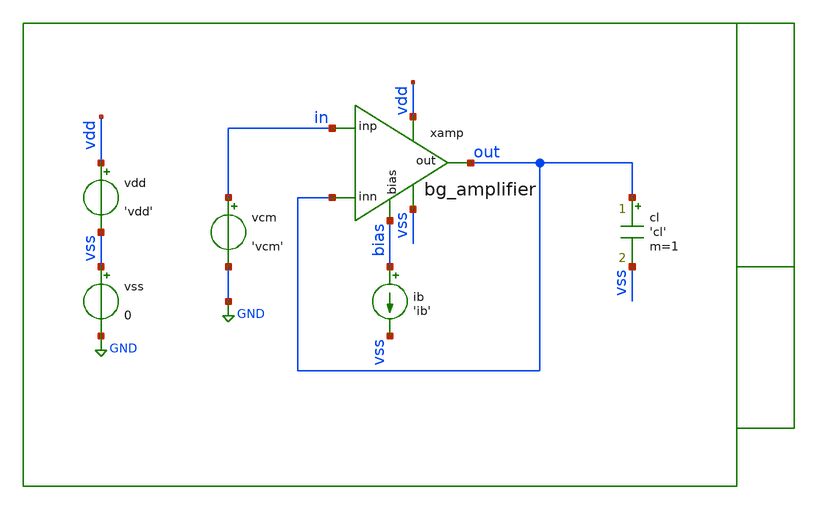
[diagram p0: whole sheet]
** sch_path: xschem/tb/bandgap_cm/bg_amplifier/mc_bg_amplifier.sch
**.subckt mc_bg_amplifier
cl out vss 'cl' m=1
vcm in GND 'vcm'
vdd vdd vss 'vdd'
vss vss GND 0
xamp vdd out in out vss bias bg_amplifier
ib bias vss 'ib'
**** begin user architecture code

* control

.param vdd=3.3
.param vcm='vdd/2'
.param ib=1u
.param cl=10p
.param rl=10e6

.control

let mc_runs   = 300
let seedvalue = 0
let steprun   = 0
let run       = 0

let vos_vec  = unitvec(mc_runs + 1)
let run_index = unitvec(mc_runs + 1)

dowhile run <= mc_runs

    alterparam sw_stat_global   = 1
    alterparam sw_stat_mismatch = 1
    reset

    save v(in) v(out)

    op

    let vos_vec[run] = v(out) - v(in)
    let run_index[run] = run

    let run = run + 1
end

setplot new
let vdiff = vos_vec
let vos = vdiff

print mean(vos)
print stddev(vos)

set wr_singlescale
set wr_vecnames
wrdata data.csv vos

.endc


 * Model Corners

.include $::CORNERS/ngspice/tt.spice
*.include $::CORNERS/ngspice/ff.spice
*.include $::CORNERS/ngspice/ss.spice
*.include $::CORNERS/ngspice/sf.spice
*.include $::CORNERS/ngspice/fs.spice

 * extract

* pex
*.include $::DESIGN_PATH/sch/bandgap_cm/bg_amplifier/bg_amplifier.pex.spice

**** end user architecture code
**.ends

* expanding   symbol:  sch/bandgap_cm/bg_amplifier/bg_amplifier.sym # of pins=6
** sym_path: xschem/sch/bandgap_cm/bg_amplifier/bg_amplifier.sym
** sch_path: xschem/sch/bandgap_cm/bg_amplifier/bg_amplifier.sch
.subckt bg_amplifier vdd out inp inn vss bias
*.ipin inn
*.ipin inp
*.opin out
*.iopin bias
*.iopin vdd
*.iopin vss
XMB5 vbn1 vbn1 vss vss nfet_06v0 L=2u W=16u nf=2 ad='int((nf+1)/2) * W/nf * 0.18u' as='int((nf+2)/2) * W/nf * 0.18u'
+ pd='2*int((nf+1)/2) * (W/nf + 0.18u)' ps='2*int((nf+2)/2) * (W/nf + 0.18u)' nrd='0.18u / W' nrs='0.18u / W'
+ sa=0 sb=0 sd=0 m=4 par=4
XMC1 von vbn1 vss vss nfet_06v0 L=2u W=16u nf=2 ad='int((nf+1)/2) * W/nf * 0.18u' as='int((nf+2)/2) * W/nf * 0.18u'
+ pd='2*int((nf+1)/2) * (W/nf + 0.18u)' ps='2*int((nf+2)/2) * (W/nf + 0.18u)' nrd='0.18u / W' nrs='0.18u / W'
+ sa=0 sb=0 sd=0 m=10 par=10
XMC2 vop vbn1 vss vss nfet_06v0 L=2u W=16u nf=2 ad='int((nf+1)/2) * W/nf * 0.18u' as='int((nf+2)/2) * W/nf * 0.18u'
+ pd='2*int((nf+1)/2) * (W/nf + 0.18u)' ps='2*int((nf+2)/2) * (W/nf + 0.18u)' nrd='0.18u / W' nrs='0.18u / W'
+ sa=0 sb=0 sd=0 m=10 par=10
XMC3 mirr vbn2 von vss nfet_06v0 L=2u W=16u nf=2 ad='int((nf+1)/2) * W/nf * 0.18u' as='int((nf+2)/2) * W/nf * 0.18u'
+ pd='2*int((nf+1)/2) * (W/nf + 0.18u)' ps='2*int((nf+2)/2) * (W/nf + 0.18u)' nrd='0.18u / W' nrs='0.18u / W'
+ sa=0 sb=0 sd=0 m=4 par=4
XMC4 out vbn2 vop vss nfet_06v0 L=2u W=16u nf=2 ad='int((nf+1)/2) * W/nf * 0.18u' as='int((nf+2)/2) * W/nf * 0.18u'
+ pd='2*int((nf+1)/2) * (W/nf + 0.18u)' ps='2*int((nf+2)/2) * (W/nf + 0.18u)' nrd='0.18u / W' nrs='0.18u / W'
+ sa=0 sb=0 sd=0 m=4 par=4
XMB3 bias bias vbp1 vdd pfet_06v0 L=2u W=16u nf=2 ad='int((nf+1)/2) * W/nf * 0.18u' as='int((nf+2)/2) * W/nf * 0.18u'
+ pd='2*int((nf+1)/2) * (W/nf + 0.18u)' ps='2*int((nf+2)/2) * (W/nf + 0.18u)' nrd='0.18u / W' nrs='0.18u / W'
+ sa=0 sb=0 sd=0 m=2 par=2
XMB1 vbp1 vbp1 vdd vdd pfet_06v0 L=2u W=16u nf=2 ad='int((nf+1)/2) * W/nf * 0.18u' as='int((nf+2)/2) * W/nf * 0.18u'
+ pd='2*int((nf+1)/2) * (W/nf + 0.18u)' ps='2*int((nf+2)/2) * (W/nf + 0.18u)' nrd='0.18u / W' nrs='0.18u / W'
+ sa=0 sb=0 sd=0 m=4 par=4
XMB2 vbn2 vbp1 vdd vdd pfet_06v0 L=2u W=16u nf=2 ad='int((nf+1)/2) * W/nf * 0.18u' as='int((nf+2)/2) * W/nf * 0.18u'
+ pd='2*int((nf+1)/2) * (W/nf + 0.18u)' ps='2*int((nf+2)/2) * (W/nf + 0.18u)' nrd='0.18u / W' nrs='0.18u / W'
+ sa=0 sb=0 sd=0 m=4 par=4
XMT1 vcm vbp1 vdd vdd pfet_06v0 L=2u W=16u nf=2 ad='int((nf+1)/2) * W/nf * 0.18u' as='int((nf+2)/2) * W/nf * 0.18u'
+ pd='2*int((nf+1)/2) * (W/nf + 0.18u)' ps='2*int((nf+2)/2) * (W/nf + 0.18u)' nrd='0.18u / W' nrs='0.18u / W'
+ sa=0 sb=0 sd=0 m=8 par=8
XMD1 von inp vcm vdd pfet_06v0 L=4u W=16u nf=2 ad='int((nf+1)/2) * W/nf * 0.18u' as='int((nf+2)/2) * W/nf * 0.18u'
+ pd='2*int((nf+1)/2) * (W/nf + 0.18u)' ps='2*int((nf+2)/2) * (W/nf + 0.18u)' nrd='0.18u / W' nrs='0.18u / W'
+ sa=0 sb=0 sd=0 m=4 par=4
XMD2 vop inn vcm vdd pfet_06v0 L=4u W=16u nf=2 ad='int((nf+1)/2) * W/nf * 0.18u' as='int((nf+2)/2) * W/nf * 0.18u'
+ pd='2*int((nf+1)/2) * (W/nf + 0.18u)' ps='2*int((nf+2)/2) * (W/nf + 0.18u)' nrd='0.18u / W' nrs='0.18u / W'
+ sa=0 sb=0 sd=0 m=4 par=4
XMC7 vda mirr vdd vdd pfet_06v0 L=2u W=16u nf=2 ad='int((nf+1)/2) * W/nf * 0.18u' as='int((nf+2)/2) * W/nf * 0.18u'
+ pd='2*int((nf+1)/2) * (W/nf + 0.18u)' ps='2*int((nf+2)/2) * (W/nf + 0.18u)' nrd='0.18u / W' nrs='0.18u / W'
+ sa=0 sb=0 sd=0 m=2 par=2
XMC8 vdb mirr vdd vdd pfet_06v0 L=2u W=16u nf=2 ad='int((nf+1)/2) * W/nf * 0.18u' as='int((nf+2)/2) * W/nf * 0.18u'
+ pd='2*int((nf+1)/2) * (W/nf + 0.18u)' ps='2*int((nf+2)/2) * (W/nf + 0.18u)' nrd='0.18u / W' nrs='0.18u / W'
+ sa=0 sb=0 sd=0 m=2 par=2
XMC5 mirr bias vda vdd pfet_06v0 L=2u W=16u nf=2 ad='int((nf+1)/2) * W/nf * 0.18u' as='int((nf+2)/2) * W/nf * 0.18u'
+ pd='2*int((nf+1)/2) * (W/nf + 0.18u)' ps='2*int((nf+2)/2) * (W/nf + 0.18u)' nrd='0.18u / W' nrs='0.18u / W'
+ sa=0 sb=0 sd=0 m=4 par=4
XMC6 out bias vdb vdd pfet_06v0 L=2u W=16u nf=2 ad='int((nf+1)/2) * W/nf * 0.18u' as='int((nf+2)/2) * W/nf * 0.18u'
+ pd='2*int((nf+1)/2) * (W/nf + 0.18u)' ps='2*int((nf+2)/2) * (W/nf + 0.18u)' nrd='0.18u / W' nrs='0.18u / W'
+ sa=0 sb=0 sd=0 m=4 par=4
XMB4 vbn2 vbn2 vbn1 vss nfet_06v0 L=2u W=16u nf=2 ad='int((nf+1)/2) * W/nf * 0.18u' as='int((nf+2)/2) * W/nf * 0.18u'
+ pd='2*int((nf+1)/2) * (W/nf + 0.18u)' ps='2*int((nf+2)/2) * (W/nf + 0.18u)' nrd='0.18u / W' nrs='0.18u / W'
+ sa=0 sb=0 sd=0 m=4 par=4
XMDUM1 vdd vdd vdd vdd pfet_06v0 L=2u W=16u nf=2 ad='int((nf+1)/2) * W/nf * 0.18u' as='int((nf+2)/2) * W/nf * 0.18u'
+ pd='2*int((nf+1)/2) * (W/nf + 0.18u)' ps='2*int((nf+2)/2) * (W/nf + 0.18u)' nrd='0.18u / W' nrs='0.18u / W'
+ sa=0 sb=0 sd=0 m=4 par=4
XMDUM2 vdd vdd vdd vdd pfet_06v0 L=2u W=16u nf=2 ad='int((nf+1)/2) * W/nf * 0.18u' as='int((nf+2)/2) * W/nf * 0.18u'
+ pd='2*int((nf+1)/2) * (W/nf + 0.18u)' ps='2*int((nf+2)/2) * (W/nf + 0.18u)' nrd='0.18u / W' nrs='0.18u / W'
+ sa=0 sb=0 sd=0 m=4 par=4
XMDUM3 vdd vdd vdd vdd pfet_06v0 L=2u W=16u nf=2 ad='int((nf+1)/2) * W/nf * 0.18u' as='int((nf+2)/2) * W/nf * 0.18u'
+ pd='2*int((nf+1)/2) * (W/nf + 0.18u)' ps='2*int((nf+2)/2) * (W/nf + 0.18u)' nrd='0.18u / W' nrs='0.18u / W'
+ sa=0 sb=0 sd=0 m=2 par=2
XMDUM4 vss vss vss vss nfet_06v0 L=2u W=16u nf=2 ad='int((nf+1)/2) * W/nf * 0.18u' as='int((nf+2)/2) * W/nf * 0.18u'
+ pd='2*int((nf+1)/2) * (W/nf + 0.18u)' ps='2*int((nf+2)/2) * (W/nf + 0.18u)' nrd='0.18u / W' nrs='0.18u / W'
+ sa=0 sb=0 sd=0 m=2 par=2
XMDUM5 vss vss vss vss nfet_06v0 L=2u W=16u nf=2 ad='int((nf+1)/2) * W/nf * 0.18u' as='int((nf+2)/2) * W/nf * 0.18u'
+ pd='2*int((nf+1)/2) * (W/nf + 0.18u)' ps='2*int((nf+2)/2) * (W/nf + 0.18u)' nrd='0.18u / W' nrs='0.18u / W'
+ sa=0 sb=0 sd=0 m=2 par=2
XMDUM6 vdd vdd vdd vdd pfet_06v0 L=4u W=16u nf=2 ad='int((nf+1)/2) * W/nf * 0.18u' as='int((nf+2)/2) * W/nf * 0.18u'
+ pd='2*int((nf+1)/2) * (W/nf + 0.18u)' ps='2*int((nf+2)/2) * (W/nf + 0.18u)' nrd='0.18u / W' nrs='0.18u / W'
+ sa=0 sb=0 sd=0 m=16 par=16
.ends

.GLOBAL GND
.end
